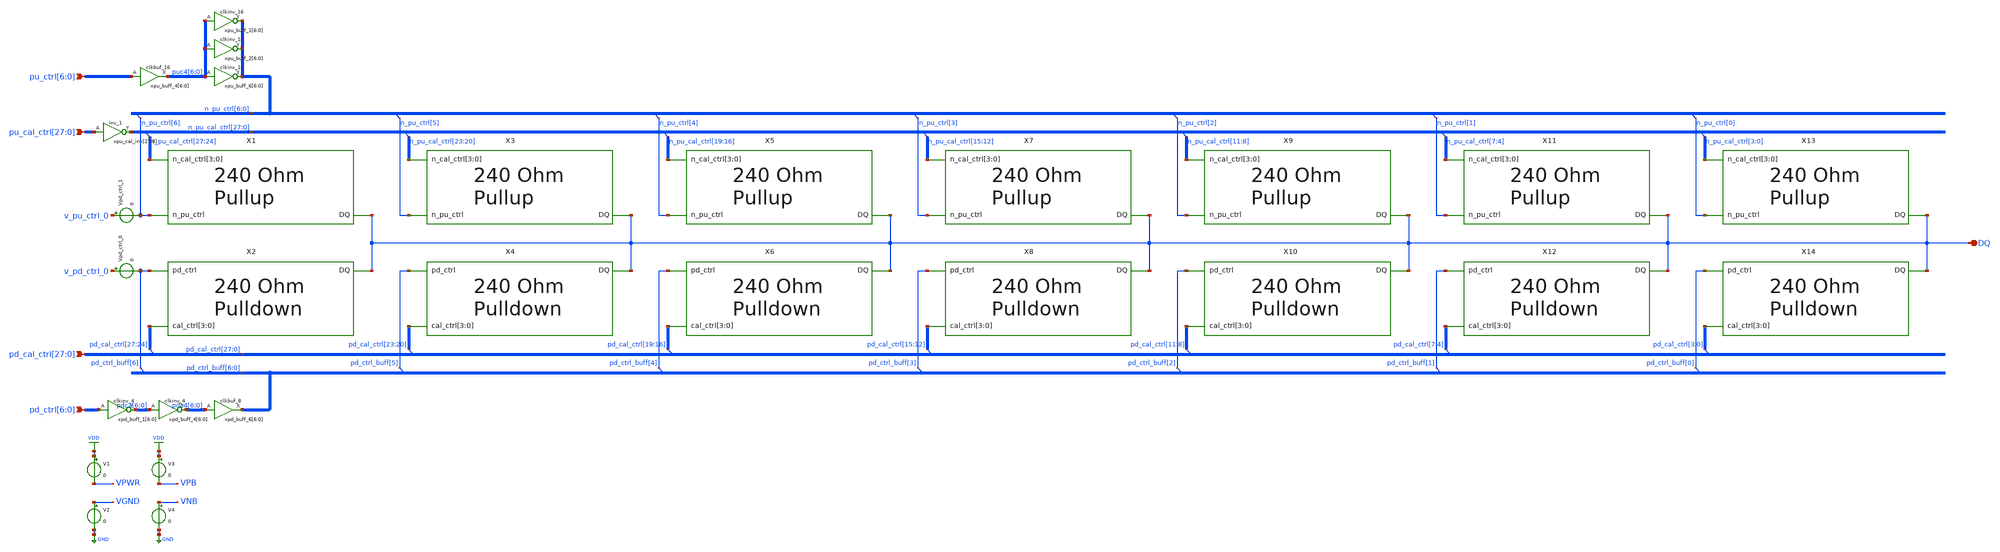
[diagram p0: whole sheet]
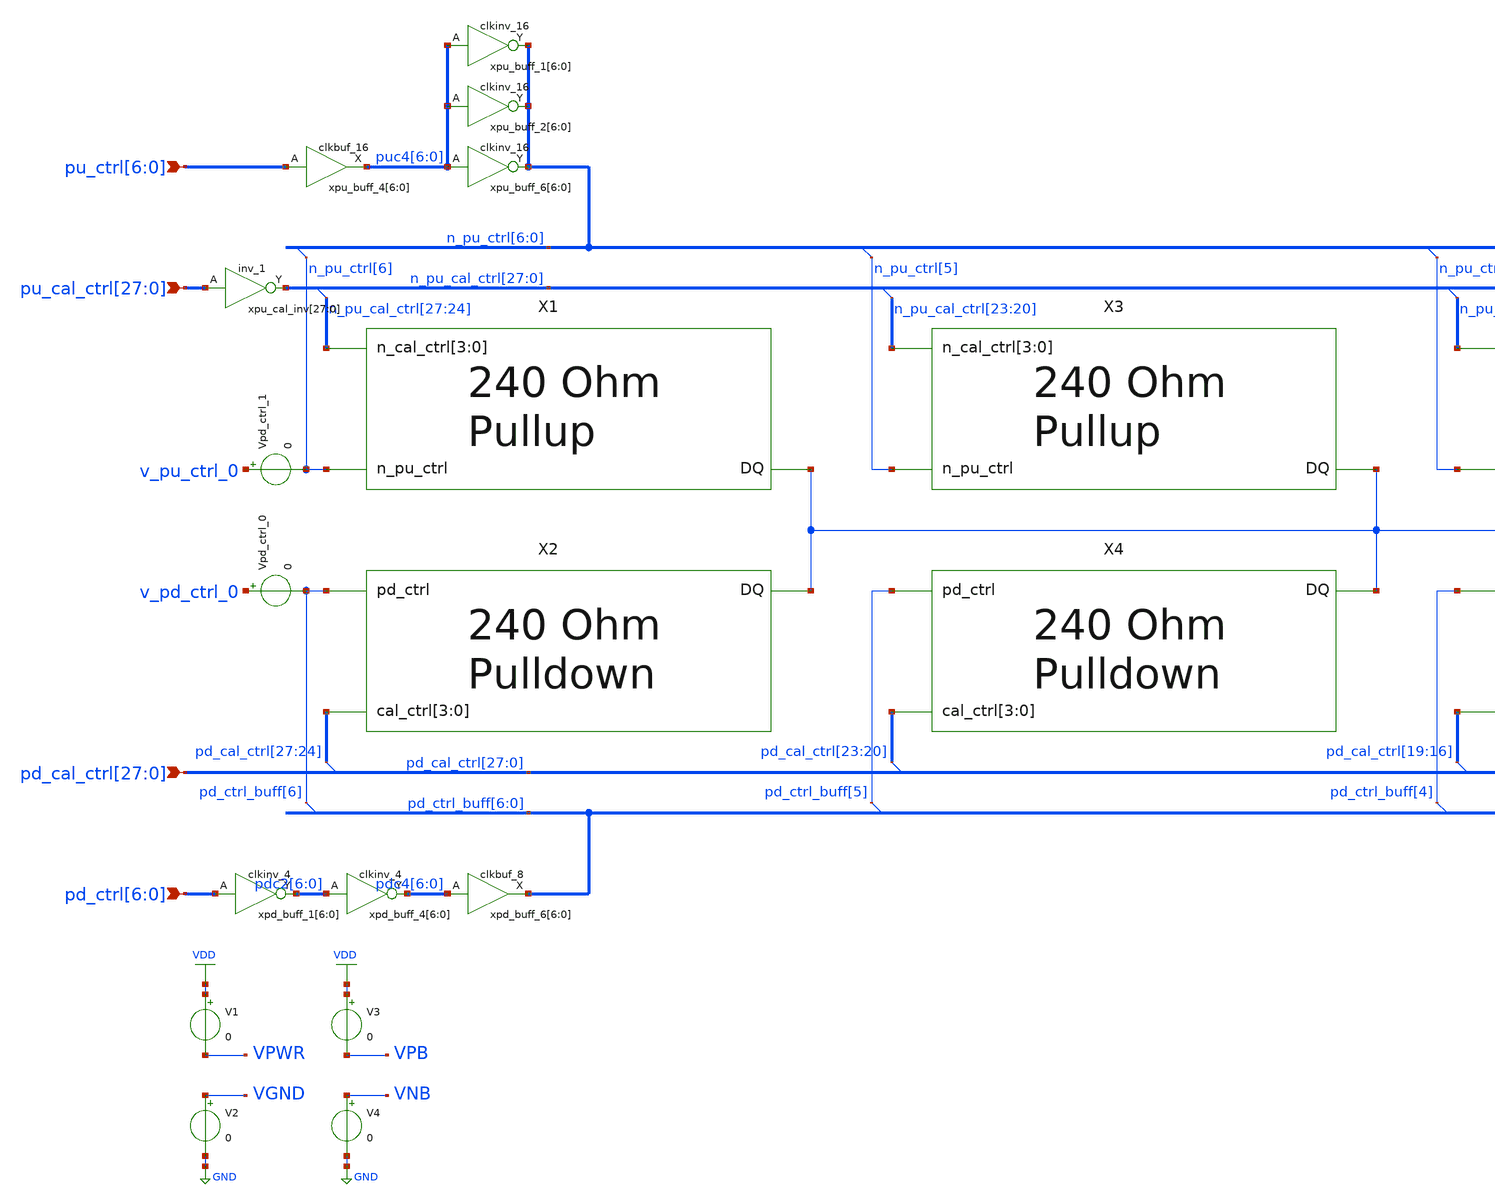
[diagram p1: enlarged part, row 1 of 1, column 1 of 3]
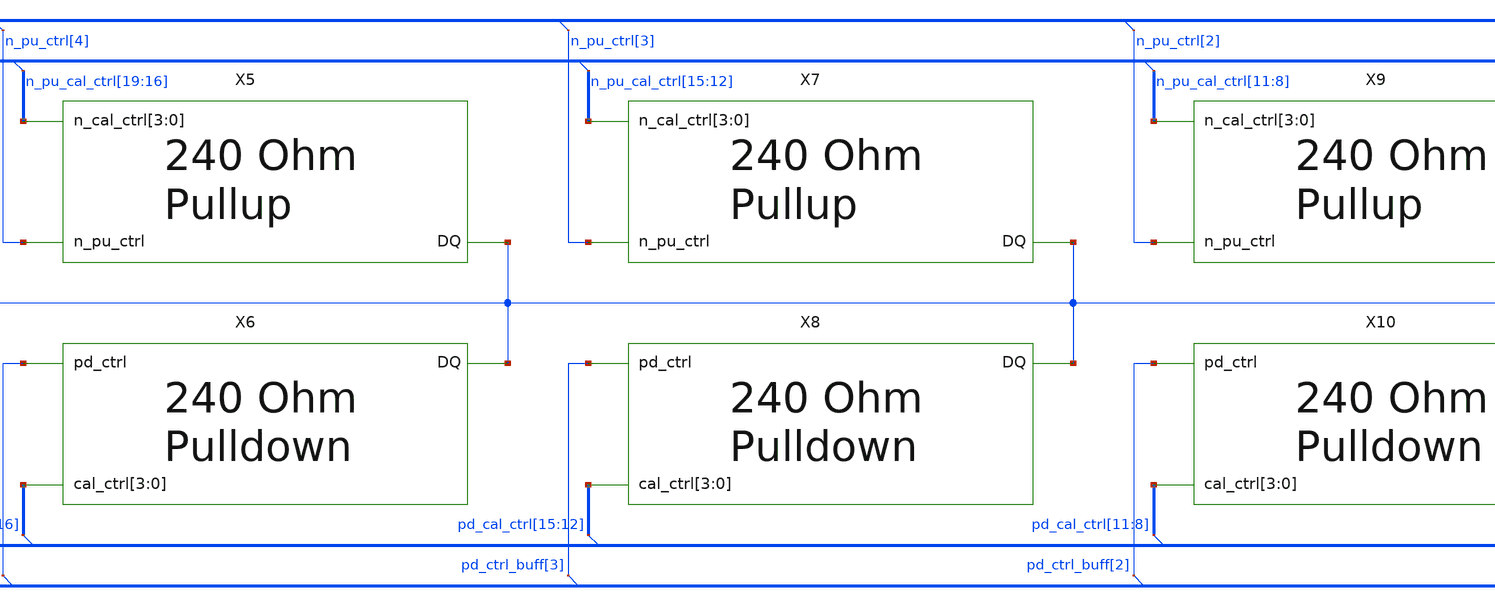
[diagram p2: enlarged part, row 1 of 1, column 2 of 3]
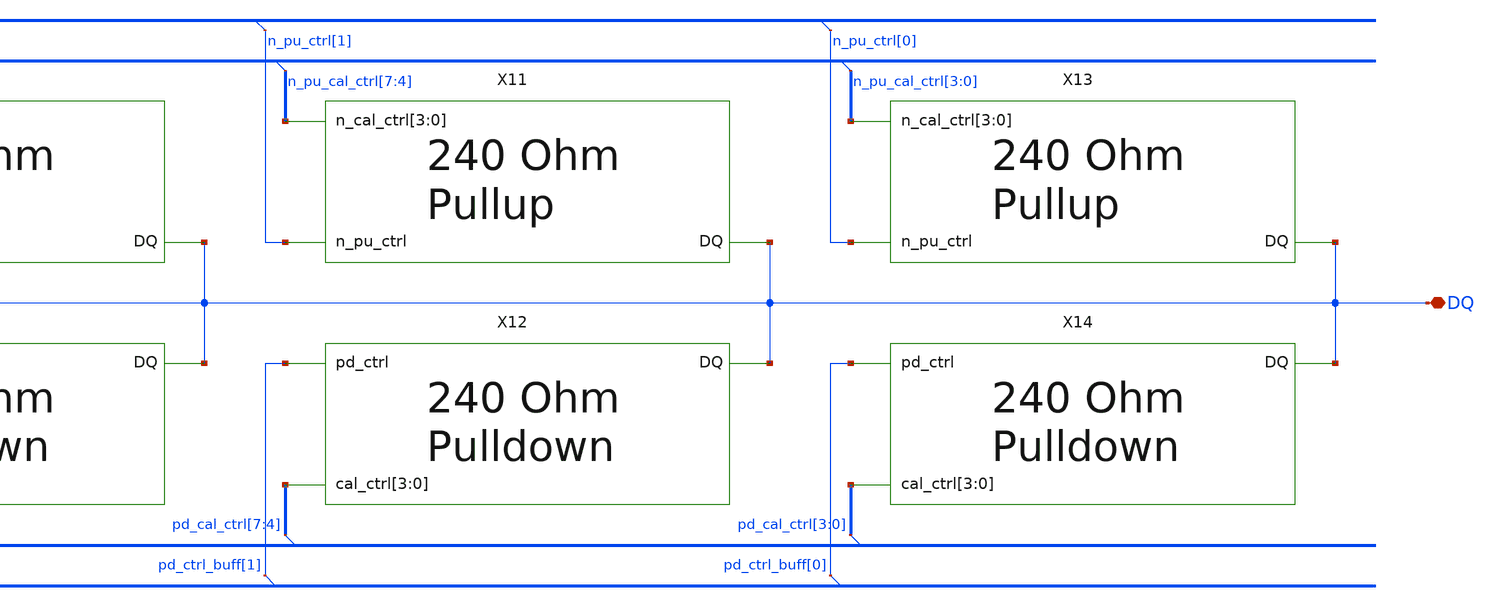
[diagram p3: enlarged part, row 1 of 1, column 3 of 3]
** sch_path: schem/SSTL.sch
* Copyright 2021 Stefan Frederik Schippers
* Licensed under the Apache License, Version 2.0 (the "License");
* you may not use this file except in compliance with the License.
* You may obtain a copy of the License at
* https://www.apache.org/licenses/LICENSE-2.0
* Unless required by applicable law or agreed to in writing, software
* distributed under the License is distributed on an "AS IS" BASIS,
* WITHOUT WARRANTIES OR CONDITIONS OF ANY KIND, either express or implied.
* See the License for the specific language governing permissions and
* limitations under the License.
**.subckt SSTL DQ
*+ pu_cal_ctrl[27],pu_cal_ctrl[26],pu_cal_ctrl[25],pu_cal_ctrl[24],pu_cal_ctrl[23],pu_cal_ctrl[22],pu_cal_ctrl[21],pu_cal_ctrl[20],pu_cal_ctrl[19],pu_cal_ctrl[18],pu_cal_ctrl[17],pu_cal_ctrl[16],pu_cal_ctrl[15],pu_cal_ctrl[14],pu_cal_ctrl[13],pu_cal_ctrl[12],pu_cal_ctrl[11],pu_cal_ctrl[10],pu_cal_ctrl[9],pu_cal_ctrl[8],pu_cal_ctrl[7],pu_cal_ctrl[6],pu_cal_ctrl[5],pu_cal_ctrl[4],pu_cal_ctrl[3],pu_cal_ctrl[2],pu_cal_ctrl[1],pu_cal_ctrl[0]
*+ pd_cal_ctrl[27],pd_cal_ctrl[26],pd_cal_ctrl[25],pd_cal_ctrl[24],pd_cal_ctrl[23],pd_cal_ctrl[22],pd_cal_ctrl[21],pd_cal_ctrl[20],pd_cal_ctrl[19],pd_cal_ctrl[18],pd_cal_ctrl[17],pd_cal_ctrl[16],pd_cal_ctrl[15],pd_cal_ctrl[14],pd_cal_ctrl[13],pd_cal_ctrl[12],pd_cal_ctrl[11],pd_cal_ctrl[10],pd_cal_ctrl[9],pd_cal_ctrl[8],pd_cal_ctrl[7],pd_cal_ctrl[6],pd_cal_ctrl[5],pd_cal_ctrl[4],pd_cal_ctrl[3],pd_cal_ctrl[2],pd_cal_ctrl[1],pd_cal_ctrl[0] pu_ctrl[6],pu_ctrl[5],pu_ctrl[4],pu_ctrl[3],pu_ctrl[2],pu_ctrl[1],pu_ctrl[0]
*+ pd_ctrl[6],pd_ctrl[5],pd_ctrl[4],pd_ctrl[3],pd_ctrl[2],pd_ctrl[1],pd_ctrl[0]
*.iopin DQ
*.ipin
*+ pu_cal_ctrl[27],pu_cal_ctrl[26],pu_cal_ctrl[25],pu_cal_ctrl[24],pu_cal_ctrl[23],pu_cal_ctrl[22],pu_cal_ctrl[21],pu_cal_ctrl[20],pu_cal_ctrl[19],pu_cal_ctrl[18],pu_cal_ctrl[17],pu_cal_ctrl[16],pu_cal_ctrl[15],pu_cal_ctrl[14],pu_cal_ctrl[13],pu_cal_ctrl[12],pu_cal_ctrl[11],pu_cal_ctrl[10],pu_cal_ctrl[9],pu_cal_ctrl[8],pu_cal_ctrl[7],pu_cal_ctrl[6],pu_cal_ctrl[5],pu_cal_ctrl[4],pu_cal_ctrl[3],pu_cal_ctrl[2],pu_cal_ctrl[1],pu_cal_ctrl[0]
*.ipin
*+ pd_cal_ctrl[27],pd_cal_ctrl[26],pd_cal_ctrl[25],pd_cal_ctrl[24],pd_cal_ctrl[23],pd_cal_ctrl[22],pd_cal_ctrl[21],pd_cal_ctrl[20],pd_cal_ctrl[19],pd_cal_ctrl[18],pd_cal_ctrl[17],pd_cal_ctrl[16],pd_cal_ctrl[15],pd_cal_ctrl[14],pd_cal_ctrl[13],pd_cal_ctrl[12],pd_cal_ctrl[11],pd_cal_ctrl[10],pd_cal_ctrl[9],pd_cal_ctrl[8],pd_cal_ctrl[7],pd_cal_ctrl[6],pd_cal_ctrl[5],pd_cal_ctrl[4],pd_cal_ctrl[3],pd_cal_ctrl[2],pd_cal_ctrl[1],pd_cal_ctrl[0]
*.ipin pu_ctrl[6],pu_ctrl[5],pu_ctrl[4],pu_ctrl[3],pu_ctrl[2],pu_ctrl[1],pu_ctrl[0]
*.ipin pd_ctrl[6],pd_ctrl[5],pd_ctrl[4],pd_ctrl[3],pd_ctrl[2],pd_ctrl[1],pd_ctrl[0]
X1 DQ n_pu_ctrl[6] n_pu_cal_ctrl[27] n_pu_cal_ctrl[26] n_pu_cal_ctrl[25] n_pu_cal_ctrl[24] p-leg
X2 DQ pd_ctrl_buff[6] pd_cal_ctrl[27] pd_cal_ctrl[26] pd_cal_ctrl[25] pd_cal_ctrl[24] n-leg
X3 DQ n_pu_ctrl[5] n_pu_cal_ctrl[23] n_pu_cal_ctrl[22] n_pu_cal_ctrl[21] n_pu_cal_ctrl[20] p-leg
X4 DQ pd_ctrl_buff[5] pd_cal_ctrl[23] pd_cal_ctrl[22] pd_cal_ctrl[21] pd_cal_ctrl[20] n-leg
X5 DQ n_pu_ctrl[4] n_pu_cal_ctrl[19] n_pu_cal_ctrl[18] n_pu_cal_ctrl[17] n_pu_cal_ctrl[16] p-leg
X6 DQ pd_ctrl_buff[4] pd_cal_ctrl[19] pd_cal_ctrl[18] pd_cal_ctrl[17] pd_cal_ctrl[16] n-leg
X7 DQ n_pu_ctrl[3] n_pu_cal_ctrl[15] n_pu_cal_ctrl[14] n_pu_cal_ctrl[13] n_pu_cal_ctrl[12] p-leg
X8 DQ pd_ctrl_buff[3] pd_cal_ctrl[15] pd_cal_ctrl[14] pd_cal_ctrl[13] pd_cal_ctrl[12] n-leg
X9 DQ n_pu_ctrl[2] n_pu_cal_ctrl[11] n_pu_cal_ctrl[10] n_pu_cal_ctrl[9] n_pu_cal_ctrl[8] p-leg
X10 DQ pd_ctrl_buff[2] pd_cal_ctrl[11] pd_cal_ctrl[10] pd_cal_ctrl[9] pd_cal_ctrl[8] n-leg
X11 DQ n_pu_ctrl[1] n_pu_cal_ctrl[7] n_pu_cal_ctrl[6] n_pu_cal_ctrl[5] n_pu_cal_ctrl[4] p-leg
X12 DQ pd_ctrl_buff[1] pd_cal_ctrl[7] pd_cal_ctrl[6] pd_cal_ctrl[5] pd_cal_ctrl[4] n-leg
X13 DQ n_pu_ctrl[0] n_pu_cal_ctrl[3] n_pu_cal_ctrl[2] n_pu_cal_ctrl[1] n_pu_cal_ctrl[0] p-leg
X14 DQ pd_ctrl_buff[0] pd_cal_ctrl[3] pd_cal_ctrl[2] pd_cal_ctrl[1] pd_cal_ctrl[0] n-leg
xpd_buff_4[6] pdc2[6] VGND VNB VPB VPWR pdc4[6] sky130_fd_sc_hd__clkinv_4
xpd_buff_4[5] pdc2[5] VGND VNB VPB VPWR pdc4[5] sky130_fd_sc_hd__clkinv_4
xpd_buff_4[4] pdc2[4] VGND VNB VPB VPWR pdc4[4] sky130_fd_sc_hd__clkinv_4
xpd_buff_4[3] pdc2[3] VGND VNB VPB VPWR pdc4[3] sky130_fd_sc_hd__clkinv_4
xpd_buff_4[2] pdc2[2] VGND VNB VPB VPWR pdc4[2] sky130_fd_sc_hd__clkinv_4
xpd_buff_4[1] pdc2[1] VGND VNB VPB VPWR pdc4[1] sky130_fd_sc_hd__clkinv_4
xpd_buff_4[0] pdc2[0] VGND VNB VPB VPWR pdc4[0] sky130_fd_sc_hd__clkinv_4
xpd_buff_6[6] pdc4[6] VGND VNB VPB VPWR pd_ctrl_buff[6] sky130_fd_sc_hd__clkbuf_8
xpd_buff_6[5] pdc4[5] VGND VNB VPB VPWR pd_ctrl_buff[5] sky130_fd_sc_hd__clkbuf_8
xpd_buff_6[4] pdc4[4] VGND VNB VPB VPWR pd_ctrl_buff[4] sky130_fd_sc_hd__clkbuf_8
xpd_buff_6[3] pdc4[3] VGND VNB VPB VPWR pd_ctrl_buff[3] sky130_fd_sc_hd__clkbuf_8
xpd_buff_6[2] pdc4[2] VGND VNB VPB VPWR pd_ctrl_buff[2] sky130_fd_sc_hd__clkbuf_8
xpd_buff_6[1] pdc4[1] VGND VNB VPB VPWR pd_ctrl_buff[1] sky130_fd_sc_hd__clkbuf_8
xpd_buff_6[0] pdc4[0] VGND VNB VPB VPWR pd_ctrl_buff[0] sky130_fd_sc_hd__clkbuf_8
xpu_buff_4[6] pu_ctrl[6] VGND VNB VPB VPWR puc4[6] sky130_fd_sc_hd__clkbuf_16
xpu_buff_4[5] pu_ctrl[5] VGND VNB VPB VPWR puc4[5] sky130_fd_sc_hd__clkbuf_16
xpu_buff_4[4] pu_ctrl[4] VGND VNB VPB VPWR puc4[4] sky130_fd_sc_hd__clkbuf_16
xpu_buff_4[3] pu_ctrl[3] VGND VNB VPB VPWR puc4[3] sky130_fd_sc_hd__clkbuf_16
xpu_buff_4[2] pu_ctrl[2] VGND VNB VPB VPWR puc4[2] sky130_fd_sc_hd__clkbuf_16
xpu_buff_4[1] pu_ctrl[1] VGND VNB VPB VPWR puc4[1] sky130_fd_sc_hd__clkbuf_16
xpu_buff_4[0] pu_ctrl[0] VGND VNB VPB VPWR puc4[0] sky130_fd_sc_hd__clkbuf_16
xpu_buff_6[6] puc4[6] VGND VNB VPB VPWR n_pu_ctrl[6] sky130_fd_sc_hd__clkinv_16
xpu_buff_6[5] puc4[5] VGND VNB VPB VPWR n_pu_ctrl[5] sky130_fd_sc_hd__clkinv_16
xpu_buff_6[4] puc4[4] VGND VNB VPB VPWR n_pu_ctrl[4] sky130_fd_sc_hd__clkinv_16
xpu_buff_6[3] puc4[3] VGND VNB VPB VPWR n_pu_ctrl[3] sky130_fd_sc_hd__clkinv_16
xpu_buff_6[2] puc4[2] VGND VNB VPB VPWR n_pu_ctrl[2] sky130_fd_sc_hd__clkinv_16
xpu_buff_6[1] puc4[1] VGND VNB VPB VPWR n_pu_ctrl[1] sky130_fd_sc_hd__clkinv_16
xpu_buff_6[0] puc4[0] VGND VNB VPB VPWR n_pu_ctrl[0] sky130_fd_sc_hd__clkinv_16
xpu_cal_inv[27] pu_cal_ctrl[27] VGND VNB VPB VPWR n_pu_cal_ctrl[27] sky130_fd_sc_hd__inv_1
xpu_cal_inv[26] pu_cal_ctrl[26] VGND VNB VPB VPWR n_pu_cal_ctrl[26] sky130_fd_sc_hd__inv_1
xpu_cal_inv[25] pu_cal_ctrl[25] VGND VNB VPB VPWR n_pu_cal_ctrl[25] sky130_fd_sc_hd__inv_1
xpu_cal_inv[24] pu_cal_ctrl[24] VGND VNB VPB VPWR n_pu_cal_ctrl[24] sky130_fd_sc_hd__inv_1
xpu_cal_inv[23] pu_cal_ctrl[23] VGND VNB VPB VPWR n_pu_cal_ctrl[23] sky130_fd_sc_hd__inv_1
xpu_cal_inv[22] pu_cal_ctrl[22] VGND VNB VPB VPWR n_pu_cal_ctrl[22] sky130_fd_sc_hd__inv_1
xpu_cal_inv[21] pu_cal_ctrl[21] VGND VNB VPB VPWR n_pu_cal_ctrl[21] sky130_fd_sc_hd__inv_1
xpu_cal_inv[20] pu_cal_ctrl[20] VGND VNB VPB VPWR n_pu_cal_ctrl[20] sky130_fd_sc_hd__inv_1
xpu_cal_inv[19] pu_cal_ctrl[19] VGND VNB VPB VPWR n_pu_cal_ctrl[19] sky130_fd_sc_hd__inv_1
xpu_cal_inv[18] pu_cal_ctrl[18] VGND VNB VPB VPWR n_pu_cal_ctrl[18] sky130_fd_sc_hd__inv_1
xpu_cal_inv[17] pu_cal_ctrl[17] VGND VNB VPB VPWR n_pu_cal_ctrl[17] sky130_fd_sc_hd__inv_1
xpu_cal_inv[16] pu_cal_ctrl[16] VGND VNB VPB VPWR n_pu_cal_ctrl[16] sky130_fd_sc_hd__inv_1
xpu_cal_inv[15] pu_cal_ctrl[15] VGND VNB VPB VPWR n_pu_cal_ctrl[15] sky130_fd_sc_hd__inv_1
xpu_cal_inv[14] pu_cal_ctrl[14] VGND VNB VPB VPWR n_pu_cal_ctrl[14] sky130_fd_sc_hd__inv_1
xpu_cal_inv[13] pu_cal_ctrl[13] VGND VNB VPB VPWR n_pu_cal_ctrl[13] sky130_fd_sc_hd__inv_1
xpu_cal_inv[12] pu_cal_ctrl[12] VGND VNB VPB VPWR n_pu_cal_ctrl[12] sky130_fd_sc_hd__inv_1
xpu_cal_inv[11] pu_cal_ctrl[11] VGND VNB VPB VPWR n_pu_cal_ctrl[11] sky130_fd_sc_hd__inv_1
xpu_cal_inv[10] pu_cal_ctrl[10] VGND VNB VPB VPWR n_pu_cal_ctrl[10] sky130_fd_sc_hd__inv_1
xpu_cal_inv[9] pu_cal_ctrl[9] VGND VNB VPB VPWR n_pu_cal_ctrl[9] sky130_fd_sc_hd__inv_1
xpu_cal_inv[8] pu_cal_ctrl[8] VGND VNB VPB VPWR n_pu_cal_ctrl[8] sky130_fd_sc_hd__inv_1
xpu_cal_inv[7] pu_cal_ctrl[7] VGND VNB VPB VPWR n_pu_cal_ctrl[7] sky130_fd_sc_hd__inv_1
xpu_cal_inv[6] pu_cal_ctrl[6] VGND VNB VPB VPWR n_pu_cal_ctrl[6] sky130_fd_sc_hd__inv_1
xpu_cal_inv[5] pu_cal_ctrl[5] VGND VNB VPB VPWR n_pu_cal_ctrl[5] sky130_fd_sc_hd__inv_1
xpu_cal_inv[4] pu_cal_ctrl[4] VGND VNB VPB VPWR n_pu_cal_ctrl[4] sky130_fd_sc_hd__inv_1
xpu_cal_inv[3] pu_cal_ctrl[3] VGND VNB VPB VPWR n_pu_cal_ctrl[3] sky130_fd_sc_hd__inv_1
xpu_cal_inv[2] pu_cal_ctrl[2] VGND VNB VPB VPWR n_pu_cal_ctrl[2] sky130_fd_sc_hd__inv_1
xpu_cal_inv[1] pu_cal_ctrl[1] VGND VNB VPB VPWR n_pu_cal_ctrl[1] sky130_fd_sc_hd__inv_1
xpu_cal_inv[0] pu_cal_ctrl[0] VGND VNB VPB VPWR n_pu_cal_ctrl[0] sky130_fd_sc_hd__inv_1
V1 VDD VPWR 0
V2 VGND GND 0
V3 VDD VPB 0
V4 VNB GND 0
Vpd_ctrl_0 v_pd_ctrl_0 pd_ctrl_buff[6] 0
Vpd_ctrl_1 v_pu_ctrl_0 n_pu_ctrl[6] 0
xpu_buff_2[6] puc4[6] VGND VNB VPB VPWR n_pu_ctrl[6] sky130_fd_sc_hd__clkinv_16
xpu_buff_2[5] puc4[5] VGND VNB VPB VPWR n_pu_ctrl[5] sky130_fd_sc_hd__clkinv_16
xpu_buff_2[4] puc4[4] VGND VNB VPB VPWR n_pu_ctrl[4] sky130_fd_sc_hd__clkinv_16
xpu_buff_2[3] puc4[3] VGND VNB VPB VPWR n_pu_ctrl[3] sky130_fd_sc_hd__clkinv_16
xpu_buff_2[2] puc4[2] VGND VNB VPB VPWR n_pu_ctrl[2] sky130_fd_sc_hd__clkinv_16
xpu_buff_2[1] puc4[1] VGND VNB VPB VPWR n_pu_ctrl[1] sky130_fd_sc_hd__clkinv_16
xpu_buff_2[0] puc4[0] VGND VNB VPB VPWR n_pu_ctrl[0] sky130_fd_sc_hd__clkinv_16
xpd_buff_1[6] pd_ctrl[6] VGND VNB VPB VPWR pdc2[6] sky130_fd_sc_hd__clkinv_4
xpd_buff_1[5] pd_ctrl[5] VGND VNB VPB VPWR pdc2[5] sky130_fd_sc_hd__clkinv_4
xpd_buff_1[4] pd_ctrl[4] VGND VNB VPB VPWR pdc2[4] sky130_fd_sc_hd__clkinv_4
xpd_buff_1[3] pd_ctrl[3] VGND VNB VPB VPWR pdc2[3] sky130_fd_sc_hd__clkinv_4
xpd_buff_1[2] pd_ctrl[2] VGND VNB VPB VPWR pdc2[2] sky130_fd_sc_hd__clkinv_4
xpd_buff_1[1] pd_ctrl[1] VGND VNB VPB VPWR pdc2[1] sky130_fd_sc_hd__clkinv_4
xpd_buff_1[0] pd_ctrl[0] VGND VNB VPB VPWR pdc2[0] sky130_fd_sc_hd__clkinv_4
xpu_buff_1[6] puc4[6] VGND VNB VPB VPWR n_pu_ctrl[6] sky130_fd_sc_hd__clkinv_16
xpu_buff_1[5] puc4[5] VGND VNB VPB VPWR n_pu_ctrl[5] sky130_fd_sc_hd__clkinv_16
xpu_buff_1[4] puc4[4] VGND VNB VPB VPWR n_pu_ctrl[4] sky130_fd_sc_hd__clkinv_16
xpu_buff_1[3] puc4[3] VGND VNB VPB VPWR n_pu_ctrl[3] sky130_fd_sc_hd__clkinv_16
xpu_buff_1[2] puc4[2] VGND VNB VPB VPWR n_pu_ctrl[2] sky130_fd_sc_hd__clkinv_16
xpu_buff_1[1] puc4[1] VGND VNB VPB VPWR n_pu_ctrl[1] sky130_fd_sc_hd__clkinv_16
xpu_buff_1[0] puc4[0] VGND VNB VPB VPWR n_pu_ctrl[0] sky130_fd_sc_hd__clkinv_16
**.ends

* expanding   symbol:  p-leg.sym # of pins=3
** sym_path: schem/p-leg.sym
** sch_path: schem/p-leg.sch
.subckt p-leg DQ n_pu_ctrl n_cal_ctrl[3] n_cal_ctrl[2] n_cal_ctrl[1] n_cal_ctrl[0]
*.ipin n_cal_ctrl[3],n_cal_ctrl[2],n_cal_ctrl[1],n_cal_ctrl[0]
*.ipin n_pu_ctrl
*.iopin DQ
XR1 DQ net1 sky130_fd_pr__res_generic_po W=0.33 L=1.8 m=1
XMpullup net1 n_pu_ctrl VDD VDD sky130_fd_pr__pfet_01v8_lvt L=0.35 W=1 nf=1 ad='int((nf+1)/2) * W/nf * 0.29'
+ as='int((nf+2)/2) * W/nf * 0.29' pd='2*int((nf+1)/2) * (W/nf + 0.29)' ps='2*int((nf+2)/2) * (W/nf + 0.29)'
+ nrd='0.29 / W' nrs='0.29 / W' sa=0 sb=0 sd=0 mult=128 m=128
XMctrltot VDD n_cal_ctrl[0] VDD VDD sky130_fd_pr__pfet_01v8_lvt L=0.35 W=1 nf=1 ad='int((nf+1)/2) * W/nf * 0.29'
+ as='int((nf+2)/2) * W/nf * 0.29' pd='2*int((nf+1)/2) * (W/nf + 0.29)' ps='2*int((nf+2)/2) * (W/nf + 0.29)'
+ nrd='0.29 / W' nrs='0.29 / W' sa=0 sb=0 sd=0 mult=120 m=120
XMctrl0 DQ n_cal_ctrl[0] net1 VDD sky130_fd_pr__pfet_01v8_lvt L=0.35 W=1 nf=1 ad='int((nf+1)/2) * W/nf * 0.29'
+ as='int((nf+2)/2) * W/nf * 0.29' pd='2*int((nf+1)/2) * (W/nf + 0.29)' ps='2*int((nf+2)/2) * (W/nf + 0.29)'
+ nrd='0.29 / W' nrs='0.29 / W' sa=0 sb=0 sd=0 mult=48 m=48
XMctrl1 DQ n_cal_ctrl[1] net1 VDD sky130_fd_pr__pfet_01v8_lvt L=0.35 W=1 nf=1 ad='int((nf+1)/2) * W/nf * 0.29'
+ as='int((nf+2)/2) * W/nf * 0.29' pd='2*int((nf+1)/2) * (W/nf + 0.29)' ps='2*int((nf+2)/2) * (W/nf + 0.29)'
+ nrd='0.29 / W' nrs='0.29 / W' sa=0 sb=0 sd=0 mult=16 m=16
XMctrl2 DQ n_cal_ctrl[2] net1 VDD sky130_fd_pr__pfet_01v8_lvt L=0.35 W=1 nf=1 ad='int((nf+1)/2) * W/nf * 0.29'
+ as='int((nf+2)/2) * W/nf * 0.29' pd='2*int((nf+1)/2) * (W/nf + 0.29)' ps='2*int((nf+2)/2) * (W/nf + 0.29)'
+ nrd='0.29 / W' nrs='0.29 / W' sa=0 sb=0 sd=0 mult=8 m=8
XMctrl3 DQ n_cal_ctrl[3] net1 VDD sky130_fd_pr__pfet_01v8_lvt L=0.35 W=1 nf=1 ad='int((nf+1)/2) * W/nf * 0.29'
+ as='int((nf+2)/2) * W/nf * 0.29' pd='2*int((nf+1)/2) * (W/nf + 0.29)' ps='2*int((nf+2)/2) * (W/nf + 0.29)'
+ nrd='0.29 / W' nrs='0.29 / W' sa=0 sb=0 sd=0 mult=4 m=4
.ends


* expanding   symbol:  n-leg.sym # of pins=3
** sym_path: schem/n-leg.sym
** sch_path: schem/n-leg.sch
.subckt n-leg DQ pd_ctrl cal_ctrl[3] cal_ctrl[2] cal_ctrl[1] cal_ctrl[0]
*.iopin DQ
*.ipin pd_ctrl
*.ipin cal_ctrl[3],cal_ctrl[2],cal_ctrl[1],cal_ctrl[0]
XR1 vpulldown DQ sky130_fd_pr__res_generic_po W=0.33 L=1.7 m=1
Xn1 vpulldown pd_ctrl GND GND sky130_fd_pr__nfet_01v8 L=0.15 W=0.65 nf=1 ad='int((nf+1)/2) * W/nf * 0.29'
+ as='int((nf+2)/2) * W/nf * 0.29' pd='2*int((nf+1)/2) * (W/nf + 0.29)' ps='2*int((nf+2)/2) * (W/nf + 0.29)'
+ nrd='0.29 / W' nrs='0.29 / W' sa=0 sb=0 sd=0 mult=48 m=48
Xnctrl0 DQ cal_ctrl[0] vpulldown GND sky130_fd_pr__nfet_01v8 L=0.15 W=0.65 nf=1 ad='int((nf+1)/2) * W/nf * 0.29'
+ as='int((nf+2)/2) * W/nf * 0.29' pd='2*int((nf+1)/2) * (W/nf + 0.29)' ps='2*int((nf+2)/2) * (W/nf + 0.29)'
+ nrd='0.29 / W' nrs='0.29 / W' sa=0 sb=0 sd=0 mult=6 m=6
Xnctrl1 DQ cal_ctrl[1] vpulldown GND sky130_fd_pr__nfet_01v8 L=0.15 W=0.65 nf=1 ad='int((nf+1)/2) * W/nf * 0.29'
+ as='int((nf+2)/2) * W/nf * 0.29' pd='2*int((nf+1)/2) * (W/nf + 0.29)' ps='2*int((nf+2)/2) * (W/nf + 0.29)'
+ nrd='0.29 / W' nrs='0.29 / W' sa=0 sb=0 sd=0 mult=3 m=3
Xnctrl2 DQ cal_ctrl[2] vpulldown GND sky130_fd_pr__nfet_01v8 L=0.15 W=0.975 nf=1 ad='int((nf+1)/2) * W/nf * 0.29'
+ as='int((nf+2)/2) * W/nf * 0.29' pd='2*int((nf+1)/2) * (W/nf + 0.29)' ps='2*int((nf+2)/2) * (W/nf + 0.29)'
+ nrd='0.29 / W' nrs='0.29 / W' sa=0 sb=0 sd=0 mult=1 m=1
Xnctrl3 DQ cal_ctrl[3] vpulldown GND sky130_fd_pr__nfet_01v8 L=0.15 W=0.5 nf=1 ad='int((nf+1)/2) * W/nf * 0.29'
+ as='int((nf+2)/2) * W/nf * 0.29' pd='2*int((nf+1)/2) * (W/nf + 0.29)' ps='2*int((nf+2)/2) * (W/nf + 0.29)'
+ nrd='0.29 / W' nrs='0.29 / W' sa=0 sb=0 sd=0 mult=1 m=1
Xnctrl_tot GND GND GND GND sky130_fd_pr__nfet_01v8 L=0.15 W=0.65 nf=1 ad='int((nf+1)/2) * W/nf * 0.29'
+ as='int((nf+2)/2) * W/nf * 0.29' pd='2*int((nf+1)/2) * (W/nf + 0.29)' ps='2*int((nf+2)/2) * (W/nf + 0.29)'
+ nrd='0.29 / W' nrs='0.29 / W' sa=0 sb=0 sd=0 mult=11 m=11
.ends

.GLOBAL VDD
.GLOBAL GND
.end
